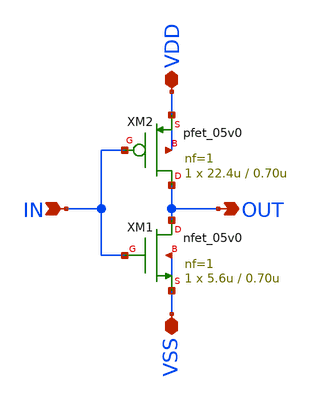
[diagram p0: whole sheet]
** sch_path: design/schematics/NOCG/SG_B11_cic_bms_afe_inv_4x.sch
**.subckt SG_B11_cic_bms_afe_inv_4x IN VDD VSS OUT
*.ipin IN
*.iopin VDD
*.iopin VSS
*.opin OUT
XM1 OUT IN VSS VSS nfet_05v0 L=0.70u W=5.6u nf=1 ad='int((nf+1)/2) * W/nf * 0.18u' as='int((nf+2)/2) * W/nf * 0.18u'
+ pd='2*int((nf+1)/2) * (W/nf + 0.18u)' ps='2*int((nf+2)/2) * (W/nf + 0.18u)' nrd='0.18u / W' nrs='0.18u / W'
+ sa=0 sb=0 sd=0 m=1
XM2 OUT IN VDD VDD pfet_05v0 L=0.70u W=22.4u nf=1 ad='int((nf+1)/2) * W/nf * 0.18u' as='int((nf+2)/2) * W/nf * 0.18u'
+ pd='2*int((nf+1)/2) * (W/nf + 0.18u)' ps='2*int((nf+2)/2) * (W/nf + 0.18u)' nrd='0.18u / W' nrs='0.18u / W'
+ sa=0 sb=0 sd=0 m=1
**.ends
.end
